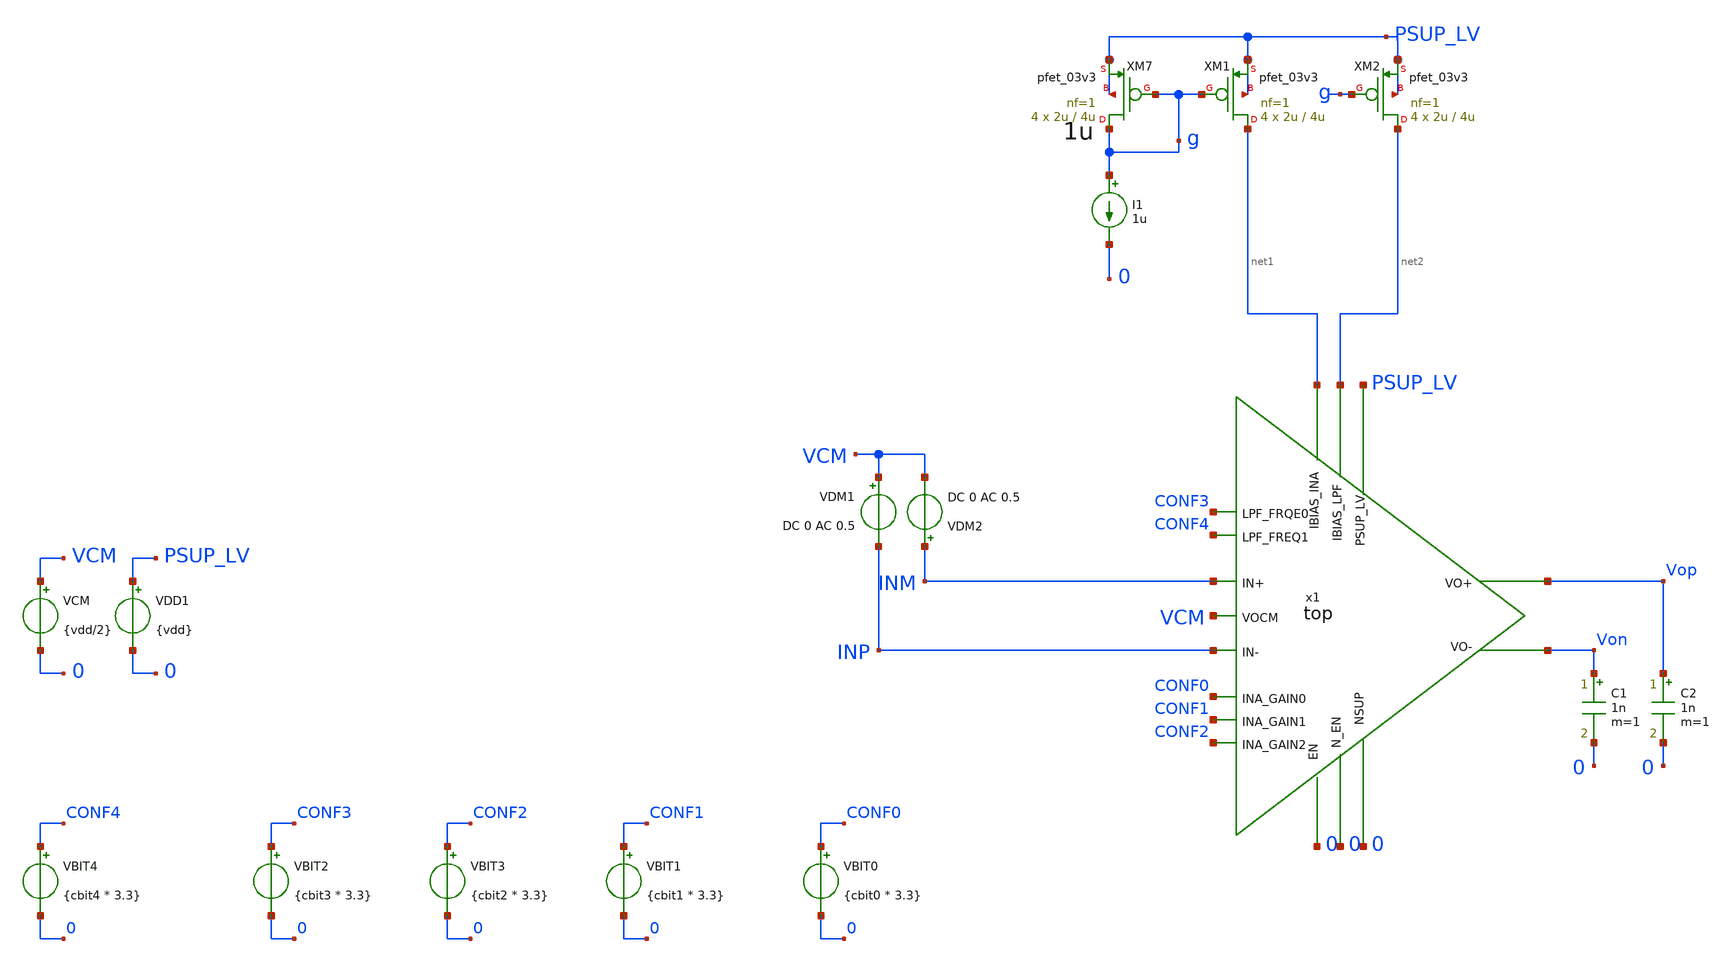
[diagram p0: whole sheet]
** sch_path: xschem/tb_top_ac.sch
**.subckt tb_top_ac
XM7 g g PSUP_LV PSUP_LV pfet_03v3 L=4u W=2u nf=1 ad='int((nf+1)/2) * W/nf * 0.18u' as='int((nf+2)/2) * W/nf * 0.18u'
+ pd='2*int((nf+1)/2) * (W/nf + 0.18u)' ps='2*int((nf+2)/2) * (W/nf + 0.18u)' nrd='0.18u / W' nrs='0.18u / W'
+ sa=0 sb=0 sd=0 m=4
XM1 net1 g PSUP_LV PSUP_LV pfet_03v3 L=4u W=2u nf=1 ad='int((nf+1)/2) * W/nf * 0.18u' as='int((nf+2)/2) * W/nf * 0.18u'
+ pd='2*int((nf+1)/2) * (W/nf + 0.18u)' ps='2*int((nf+2)/2) * (W/nf + 0.18u)' nrd='0.18u / W' nrs='0.18u / W'
+ sa=0 sb=0 sd=0 m=4
I1 g 0 1u
XM2 net2 g PSUP_LV PSUP_LV pfet_03v3 L=4u W=2u nf=1 ad='int((nf+1)/2) * W/nf * 0.18u' as='int((nf+2)/2) * W/nf * 0.18u'
+ pd='2*int((nf+1)/2) * (W/nf + 0.18u)' ps='2*int((nf+2)/2) * (W/nf + 0.18u)' nrd='0.18u / W' nrs='0.18u / W'
+ sa=0 sb=0 sd=0 m=4
VDM2 INM VCM DC 0 AC 0.5
VDM1 VCM INP DC 0 AC 0.5
C1 Von 0 1n m=1
C2 Vop 0 1n m=1
VBIT1 CONF1 0 {cbit1 * 3.3}
VBIT0 CONF0 0 {cbit0 * 3.3}
VBIT2 CONF3 0 {cbit3 * 3.3}
VBIT3 CONF2 0 {cbit2 * 3.3}
VBIT4 CONF4 0 {cbit4 * 3.3}
VDD1 PSUP_LV 0 {vdd}
VCM VCM 0 {vdd/2}
x1 PSUP_LV 0 net2 INM Vop INP Von CONF4 CONF1 CONF3 CONF0 CONF2 net1 VCM 0 0 top
**** begin user architecture code

.include $::180MCU_MODELS/design.ngspice

.lib $::180MCU_MODELS/sm141064.ngspice typical
.lib $::180MCU_MODELS/sm141064.ngspice res_typical
.lib $::180MCU_MODELS/sm141064.ngspice bjt_typical
.lib $::180MCU_MODELS/sm141064.ngspice mimcap_typical
.lib $::180MCU_MODELS/sm141064.ngspice cap_mim

.temp 25

.param vdd=3.3

.param cbit0=0
.param cbit1=0
.param cbit2=0
.param cbit3=0
.param cbit4=0

* Deterministic PVT: disable random global/mismatch variation.
.param sw_stat_global=0
.param sw_stat_mismatch=0



.control
set units=degrees
save all
ac dec 100 1 1G

let Vid = v(INP) - v(INM)
let Vo = v(Vop) - v(Von)
let aol = v(Vo) / v(Vid)
let gain_db = db(aol)
let phase_deg = cph(aol)

write tb_top_ac.raw gain_db phase_deg

.endc


**** end user architecture code
**.ends
.end
